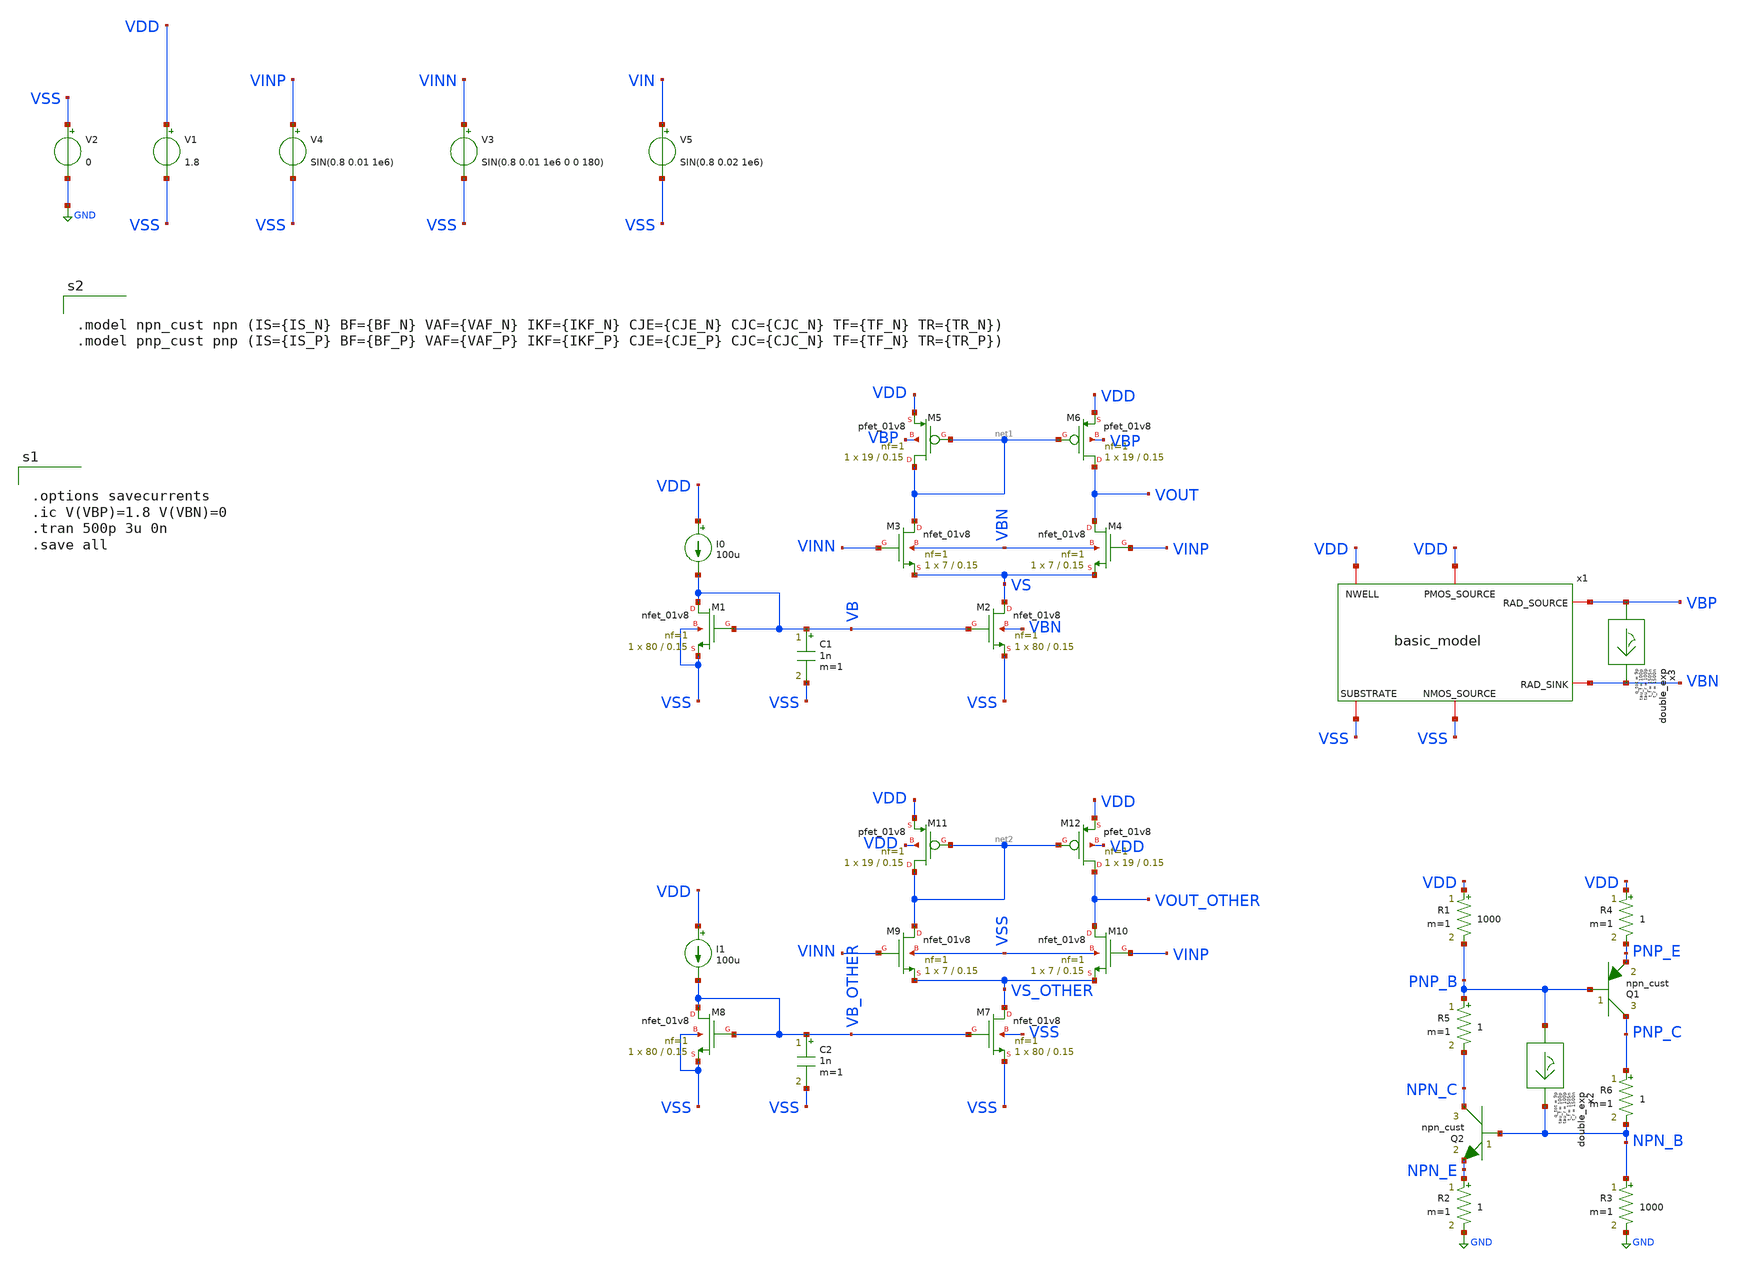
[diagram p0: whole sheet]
** sch_path: untitled-7.sch
**.subckt untitled-7
XM2 VS VB VSS VBN sky130_fd_pr__nfet_01v8 L=0.15 W=80 nf=1 ad='int((nf+1)/2) * W/nf * 0.29' as='int((nf+2)/2) * W/nf * 0.29'
+ pd='2*int((nf+1)/2) * (W/nf + 0.29)' ps='2*int((nf+2)/2) * (W/nf + 0.29)' nrd='0.29 / W' nrs='0.29 / W'
+ sa=0 sb=0 sd=0 mult=1 m=1
V1 VDD VSS 1.8
V2 VSS GND 0
XM1 VB VB VSS VSS sky130_fd_pr__nfet_01v8 L=0.15 W=80 nf=1 ad='int((nf+1)/2) * W/nf * 0.29' as='int((nf+2)/2) * W/nf * 0.29'
+ pd='2*int((nf+1)/2) * (W/nf + 0.29)' ps='2*int((nf+2)/2) * (W/nf + 0.29)' nrd='0.29 / W' nrs='0.29 / W'
+ sa=0 sb=0 sd=0 mult=1 m=1
I0 VDD VB 100u
XM3 net1 VINN VS VBN sky130_fd_pr__nfet_01v8 L=0.15 W=7 nf=1 ad='int((nf+1)/2) * W/nf * 0.29' as='int((nf+2)/2) * W/nf * 0.29'
+ pd='2*int((nf+1)/2) * (W/nf + 0.29)' ps='2*int((nf+2)/2) * (W/nf + 0.29)' nrd='0.29 / W' nrs='0.29 / W'
+ sa=0 sb=0 sd=0 mult=1 m=1
XM4 VOUT VINP VS VBN sky130_fd_pr__nfet_01v8 L=0.15 W=7 nf=1 ad='int((nf+1)/2) * W/nf * 0.29' as='int((nf+2)/2) * W/nf * 0.29'
+ pd='2*int((nf+1)/2) * (W/nf + 0.29)' ps='2*int((nf+2)/2) * (W/nf + 0.29)' nrd='0.29 / W' nrs='0.29 / W'
+ sa=0 sb=0 sd=0 mult=1 m=1
XM5 net1 net1 VDD VBP sky130_fd_pr__pfet_01v8 L=0.15 W=19 nf=1 ad='int((nf+1)/2) * W/nf * 0.29' as='int((nf+2)/2) * W/nf * 0.29'
+ pd='2*int((nf+1)/2) * (W/nf + 0.29)' ps='2*int((nf+2)/2) * (W/nf + 0.29)' nrd='0.29 / W' nrs='0.29 / W'
+ sa=0 sb=0 sd=0 mult=1 m=1
XM6 VOUT net1 VDD VBP sky130_fd_pr__pfet_01v8 L=0.15 W=19 nf=1 ad='int((nf+1)/2) * W/nf * 0.29' as='int((nf+2)/2) * W/nf * 0.29'
+ pd='2*int((nf+1)/2) * (W/nf + 0.29)' ps='2*int((nf+2)/2) * (W/nf + 0.29)' nrd='0.29 / W' nrs='0.29 / W'
+ sa=0 sb=0 sd=0 mult=1 m=1
V4 VINP VSS SIN(0.8 0.01 1e6)
V3 VINN VSS SIN(0.8 0.01 1e6 0 0 180)
C1 VB VSS 1n m=1
x3 VBP VBN double_exp t_r=1500n tau_r=100p t_f=1505n tau_f=100p q_tot=9p
x1 VDD VDD VBP VBN VSS VSS basic_model
V5 VIN VSS SIN(0.8 0.02 1e6)
XM7 VS_OTHER VB_OTHER VSS VSS sky130_fd_pr__nfet_01v8 L=0.15 W=80 nf=1 ad='int((nf+1)/2) * W/nf * 0.29'
+ as='int((nf+2)/2) * W/nf * 0.29' pd='2*int((nf+1)/2) * (W/nf + 0.29)' ps='2*int((nf+2)/2) * (W/nf + 0.29)'
+ nrd='0.29 / W' nrs='0.29 / W' sa=0 sb=0 sd=0 mult=1 m=1
XM8 VB_OTHER VB_OTHER VSS VSS sky130_fd_pr__nfet_01v8 L=0.15 W=80 nf=1 ad='int((nf+1)/2) * W/nf * 0.29'
+ as='int((nf+2)/2) * W/nf * 0.29' pd='2*int((nf+1)/2) * (W/nf + 0.29)' ps='2*int((nf+2)/2) * (W/nf + 0.29)'
+ nrd='0.29 / W' nrs='0.29 / W' sa=0 sb=0 sd=0 mult=1 m=1
I1 VDD VB_OTHER 100u
XM9 net2 VINN VS_OTHER VSS sky130_fd_pr__nfet_01v8 L=0.15 W=7 nf=1 ad='int((nf+1)/2) * W/nf * 0.29' as='int((nf+2)/2) * W/nf * 0.29'
+ pd='2*int((nf+1)/2) * (W/nf + 0.29)' ps='2*int((nf+2)/2) * (W/nf + 0.29)' nrd='0.29 / W' nrs='0.29 / W'
+ sa=0 sb=0 sd=0 mult=1 m=1
XM10 VOUT_OTHER VINP VS_OTHER VSS sky130_fd_pr__nfet_01v8 L=0.15 W=7 nf=1 ad='int((nf+1)/2) * W/nf * 0.29'
+ as='int((nf+2)/2) * W/nf * 0.29' pd='2*int((nf+1)/2) * (W/nf + 0.29)' ps='2*int((nf+2)/2) * (W/nf + 0.29)'
+ nrd='0.29 / W' nrs='0.29 / W' sa=0 sb=0 sd=0 mult=1 m=1
XM11 net2 net2 VDD VDD sky130_fd_pr__pfet_01v8 L=0.15 W=19 nf=1 ad='int((nf+1)/2) * W/nf * 0.29' as='int((nf+2)/2) * W/nf * 0.29'
+ pd='2*int((nf+1)/2) * (W/nf + 0.29)' ps='2*int((nf+2)/2) * (W/nf + 0.29)' nrd='0.29 / W' nrs='0.29 / W'
+ sa=0 sb=0 sd=0 mult=1 m=1
XM12 VOUT_OTHER net2 VDD VDD sky130_fd_pr__pfet_01v8 L=0.15 W=19 nf=1 ad='int((nf+1)/2) * W/nf * 0.29'
+ as='int((nf+2)/2) * W/nf * 0.29' pd='2*int((nf+1)/2) * (W/nf + 0.29)' ps='2*int((nf+2)/2) * (W/nf + 0.29)'
+ nrd='0.29 / W' nrs='0.29 / W' sa=0 sb=0 sd=0 mult=1 m=1
C2 VB_OTHER VSS 1n m=1
Q1 PNP_C PNP_B PNP_E npn_cust area=1 m=1
Q2 NPN_C NPN_B NPN_E npn_cust area=1 m=1
R3 NPN_B GND 1000 m=1
R4 VDD PNP_E 1 m=1
R1 VDD PNP_B 1000 m=1
R2 NPN_E GND 1 m=1
R5 PNP_B NPN_C 1 m=1
R6 PNP_C NPN_B 1 m=1
x2 PNP_B NPN_B double_exp t_r=1500n tau_r=100p t_f=1505n tau_f=100p q_tot=9p
**** begin user architecture code


.options savecurrents
.ic V(VBP)=1.8 V(VBN)=0
.tran 500p 3u 0n
.save all



** opencircuitdesign pdks install
.lib $::SKYWATER_MODELS/sky130.lib.spice tt




.include /usr/local/share/rad_modeling_blocks/rad_modeling_blocks.spice




.model npn_cust npn (IS={IS_N} BF={BF_N} VAF={VAF_N} IKF={IKF_N} CJE={CJE_N} CJC={CJC_N} TF={TF_N} TR={TR_N})
.model pnp_cust pnp (IS={IS_P} BF={BF_P} VAF={VAF_P} IKF={IKF_P} CJE={CJE_P} CJC={CJC_N} TF={TF_N} TR={TR_P})


**** end user architecture code
**.ends

* expanding   symbol:  double_exp.sym # of pins=2
** sym_path: xschem_rad_library/double_exp.sym
** sch_path: xschem_rad_library/double_exp.sch
.subckt double_exp in out  t_r=0 t_f=0 tau_r=0 tau_f=0 q_tot=0
*.opin OUT
*.ipin IN
I1 IN OUT EXP(0 {q_tot / (t_f-t_r+tau_f-tau_r)} {t_r} {tau_r} {t_f} {tau_f})
.ends


* expanding   symbol:  OSCRE/latchup/basic_model.sym # of pins=6
** sym_path: latchup/basic_model.sym
** sch_path: latchup/basic_model.sch
.subckt basic_model PMOS_SOURCE NWELL RAD_SOURCE RAD_SINK NMOS_SOURCE SUBSTRATE   IS_N=1e-18
+  BF_N=100  VAF_N=50  IKF_N=0.01  CJE_N=0.2p  CJC_N=0.1p  TF_N=0.2n  TR_N=2n  IS_P=1e-18  BF_P=100  VAF_P=50
+  IKF_P=0.01  CJE_P=0.3p  CJC_P=0.15p  TF_P=0.3n  TR_P=3n
*.iopin NWELL
*.iopin SUBSTRATE
*.iopin RAD_SOURCE
*.iopin RAD_SINK
*.iopin NMOS_SOURCE
*.iopin PMOS_SOURCE
Q1 RAD_SINK RAD_SOURCE PMOS_SOURCE pnp_cust area=1 m=1
Q2 RAD_SOURCE RAD_SINK NMOS_SOURCE npn_cust area=1 m=1
R3 RAD_SINK SUBSTRATE 1000 m=1
R4 NWELL RAD_SOURCE 1000 m=1
**** begin user architecture code


.model npn_cust npn (IS={IS_N} BF={BF_N} VAF={VAF_N} IKF={IKF_N} CJE={CJE_N} CJC={CJC_N} TF={TF_N} TR={TR_N})
.model pnp_cust pnp (IS={IS_P} BF={BF_P} VAF={VAF_P} IKF={IKF_P} CJE={CJE_P} CJC={CJC_N} TF={TF_N} TR={TR_P})


**** end user architecture code
.ends

.GLOBAL GND
.end
